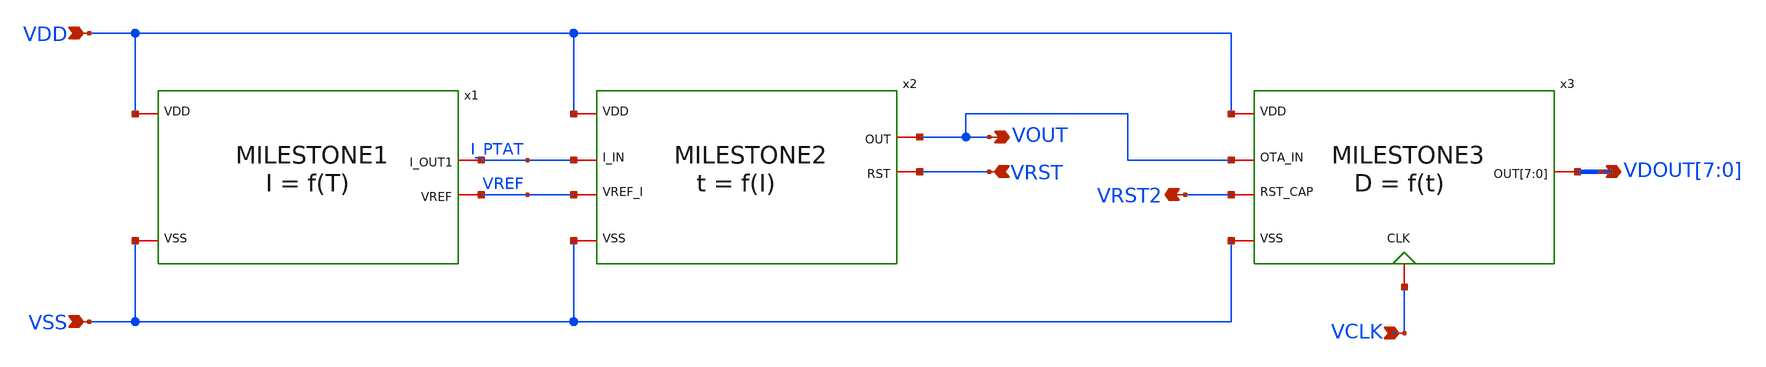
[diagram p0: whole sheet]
** sch_path: design/CNR_GR03_SKY130NM/TOPLEVEL.sch
**.subckt TOPLEVEL VDD VSS VOUT VRST
*+ VDOUT[7],VDOUT[6],VDOUT[5],VDOUT[4],VDOUT[3],VDOUT[2],VDOUT[1],VDOUT[0] VRST2 VCLK
*.ipin VDD
*.ipin VSS
*.opin VOUT
*.ipin VRST
*.opin VDOUT[7],VDOUT[6],VDOUT[5],VDOUT[4],VDOUT[3],VDOUT[2],VDOUT[1],VDOUT[0]
*.opin VRST2
*.ipin VCLK
x1 VDD I_PTAT VREF VSS MILESTONE1
x2 I_PTAT VREF VOUT VDD VRST VSS MILESTONE2
x3 VOUT VRST2 VCLK VDOUT[7] VDOUT[6] VDOUT[5] VDOUT[4] VDOUT[3] VDOUT[2] VDOUT[1] VDOUT[0] VDD VSS
+ MILESTONE3
**.ends
.end
